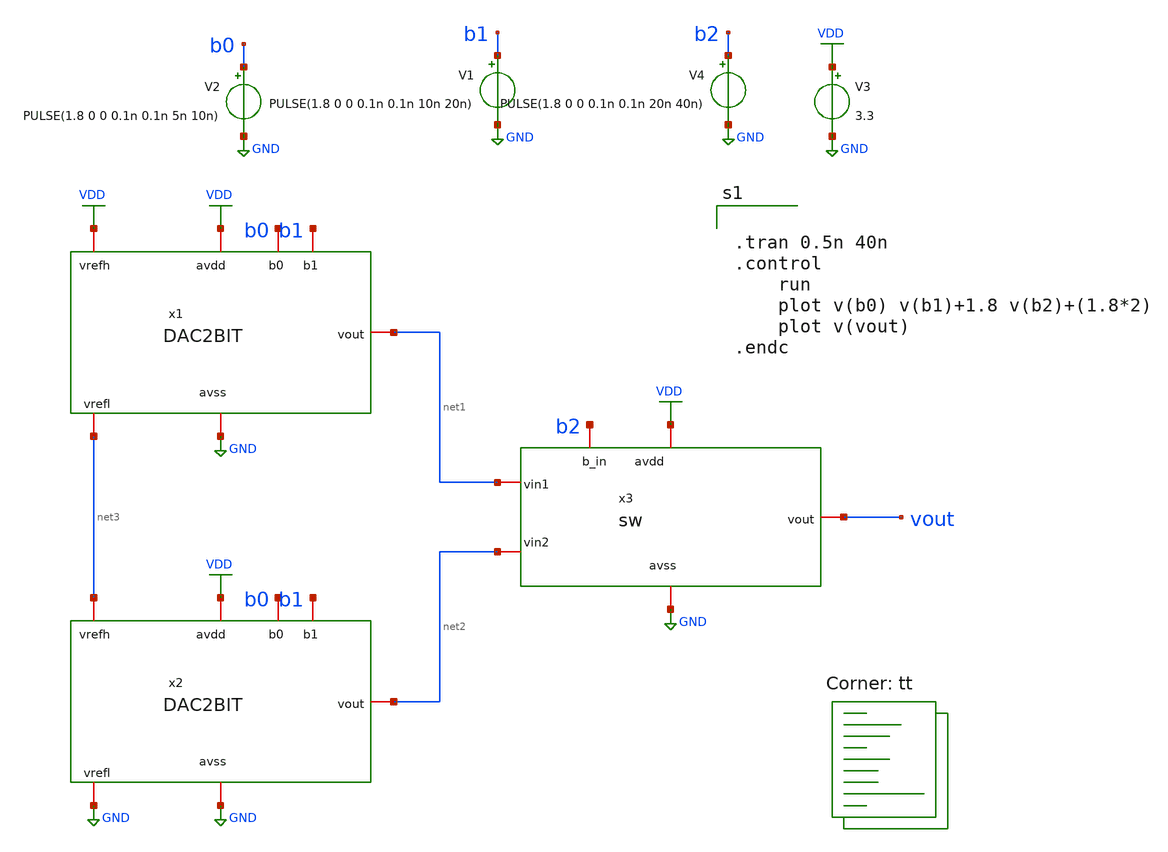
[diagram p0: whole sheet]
** sch_path: designs/libs/crossmem_ipn/dac4bits/sch/tb_DAC3BIT.sch
**.subckt tb_DAC3BIT
x1 b0 VDD b1 GND VDD net1 net3 DAC2BIT
x2 b0 VDD b1 GND net3 net2 GND DAC2BIT
x3 VDD b2 GND net1 vout net2 sw
V2 b0 GND PULSE(1.8 0 0 0.1n 0.1n 5n 10n)
V1 b1 GND PULSE(1.8 0 0 0.1n 0.1n 10n 20n)
V3 VDD GND 3.3
V4 b2 GND PULSE(1.8 0 0 0.1n 0.1n 20n 40n)
**** begin user architecture code
.lib $::SKYWATER_MODELS/sky130.lib.spice tt


.tran 0.5n 40n
.control
	run
	plot v(b0) v(b1)+1.8 v(b2)+(1.8*2)
	plot v(vout)
.endc



**** end user architecture code
**.ends

* expanding   symbol:  DAC2BIT.sym # of pins=7
** sym_path: designs/libs/crossmem_ipn/dac4bits/sch/DAC2BIT.sym
** sch_path: designs/libs/crossmem_ipn/dac4bits/sch/DAC2BIT.sch
.subckt DAC2BIT b0 avdd b1 avss vrefh vout vrefl
*.iopin vrefh
*.iopin vrefl
*.iopin b0
*.iopin b1
*.iopin avdd
*.iopin avss
*.iopin vout
x1 avdd b0 avss net5 net1 net4 sw
x2 avdd b0 avss net3 net2 vrefl sw
x3 avdd b1 avss net1 vout net2 sw
R5 net5 vrefh sky130_fd_pr__res_generic_l1 W=1 L=3.75 m=1
R6 net4 net5 sky130_fd_pr__res_generic_l1 W=1 L=3.75 m=1
R7 net3 net4 sky130_fd_pr__res_generic_l1 W=1 L=3.75 m=1
R8 vrefl net3 sky130_fd_pr__res_generic_l1 W=1 L=3.75 m=1
.ends


* expanding   symbol:  sw.sym # of pins=6
** sym_path: designs/libs/crossmem_ipn/dac4bits/sch/sw.sym
** sch_path: designs/libs/crossmem_ipn/dac4bits/sch/sw.sch
.subckt sw avdd b_in avss vin1 vout vin2
*.iopin avss
*.iopin vin1
*.iopin vout
*.iopin avdd
*.iopin vin2
*.iopin b_in
XM1 net1 b_in avss avss sky130_fd_pr__nfet_01v8 L=0.15 W=0.5 nf=1 ad='int((nf+1)/2) * W/nf * 0.29' as='int((nf+2)/2) * W/nf * 0.29'
+ pd='2*int((nf+1)/2) * (W/nf + 0.29)' ps='2*int((nf+2)/2) * (W/nf + 0.29)' nrd='0.29 / W' nrs='0.29 / W'
+ sa=0 sb=0 sd=0 mult=1 m=1
XM2 net1 b_in avdd avdd sky130_fd_pr__pfet_01v8 L=0.15 W=0.5 nf=1 ad='int((nf+1)/2) * W/nf * 0.29' as='int((nf+2)/2) * W/nf * 0.29'
+ pd='2*int((nf+1)/2) * (W/nf + 0.29)' ps='2*int((nf+2)/2) * (W/nf + 0.29)' nrd='0.29 / W' nrs='0.29 / W'
+ sa=0 sb=0 sd=0 mult=1 m=1
XM3 net2 net1 avss avss sky130_fd_pr__nfet_01v8 L=0.15 W=0.5 nf=1 ad='int((nf+1)/2) * W/nf * 0.29' as='int((nf+2)/2) * W/nf * 0.29'
+ pd='2*int((nf+1)/2) * (W/nf + 0.29)' ps='2*int((nf+2)/2) * (W/nf + 0.29)' nrd='0.29 / W' nrs='0.29 / W'
+ sa=0 sb=0 sd=0 mult=1 m=1
XM4 net2 net1 avdd avdd sky130_fd_pr__pfet_01v8 L=0.15 W=0.5 nf=1 ad='int((nf+1)/2) * W/nf * 0.29' as='int((nf+2)/2) * W/nf * 0.29'
+ pd='2*int((nf+1)/2) * (W/nf + 0.29)' ps='2*int((nf+2)/2) * (W/nf + 0.29)' nrd='0.29 / W' nrs='0.29 / W'
+ sa=0 sb=0 sd=0 mult=1 m=1
XM5 vout net1 vin1 avdd sky130_fd_pr__pfet_01v8 L=0.15 W=0.5 nf=1 ad='int((nf+1)/2) * W/nf * 0.29' as='int((nf+2)/2) * W/nf * 0.29'
+ pd='2*int((nf+1)/2) * (W/nf + 0.29)' ps='2*int((nf+2)/2) * (W/nf + 0.29)' nrd='0.29 / W' nrs='0.29 / W'
+ sa=0 sb=0 sd=0 mult=1 m=1
XM6 vout net1 vin2 avss sky130_fd_pr__nfet_01v8 L=0.15 W=0.5 nf=1 ad='int((nf+1)/2) * W/nf * 0.29' as='int((nf+2)/2) * W/nf * 0.29'
+ pd='2*int((nf+1)/2) * (W/nf + 0.29)' ps='2*int((nf+2)/2) * (W/nf + 0.29)' nrd='0.29 / W' nrs='0.29 / W'
+ sa=0 sb=0 sd=0 mult=1 m=1
XM7 vin1 net2 vout avss sky130_fd_pr__nfet_01v8 L=0.15 W=0.5 nf=1 ad='int((nf+1)/2) * W/nf * 0.29' as='int((nf+2)/2) * W/nf * 0.29'
+ pd='2*int((nf+1)/2) * (W/nf + 0.29)' ps='2*int((nf+2)/2) * (W/nf + 0.29)' nrd='0.29 / W' nrs='0.29 / W'
+ sa=0 sb=0 sd=0 mult=1 m=1
XM8 vin2 net2 vout avdd sky130_fd_pr__pfet_01v8 L=0.15 W=0.5 nf=1 ad='int((nf+1)/2) * W/nf * 0.29' as='int((nf+2)/2) * W/nf * 0.29'
+ pd='2*int((nf+1)/2) * (W/nf + 0.29)' ps='2*int((nf+2)/2) * (W/nf + 0.29)' nrd='0.29 / W' nrs='0.29 / W'
+ sa=0 sb=0 sd=0 mult=1 m=1
.ends

.GLOBAL GND
.GLOBAL VDD
.end
